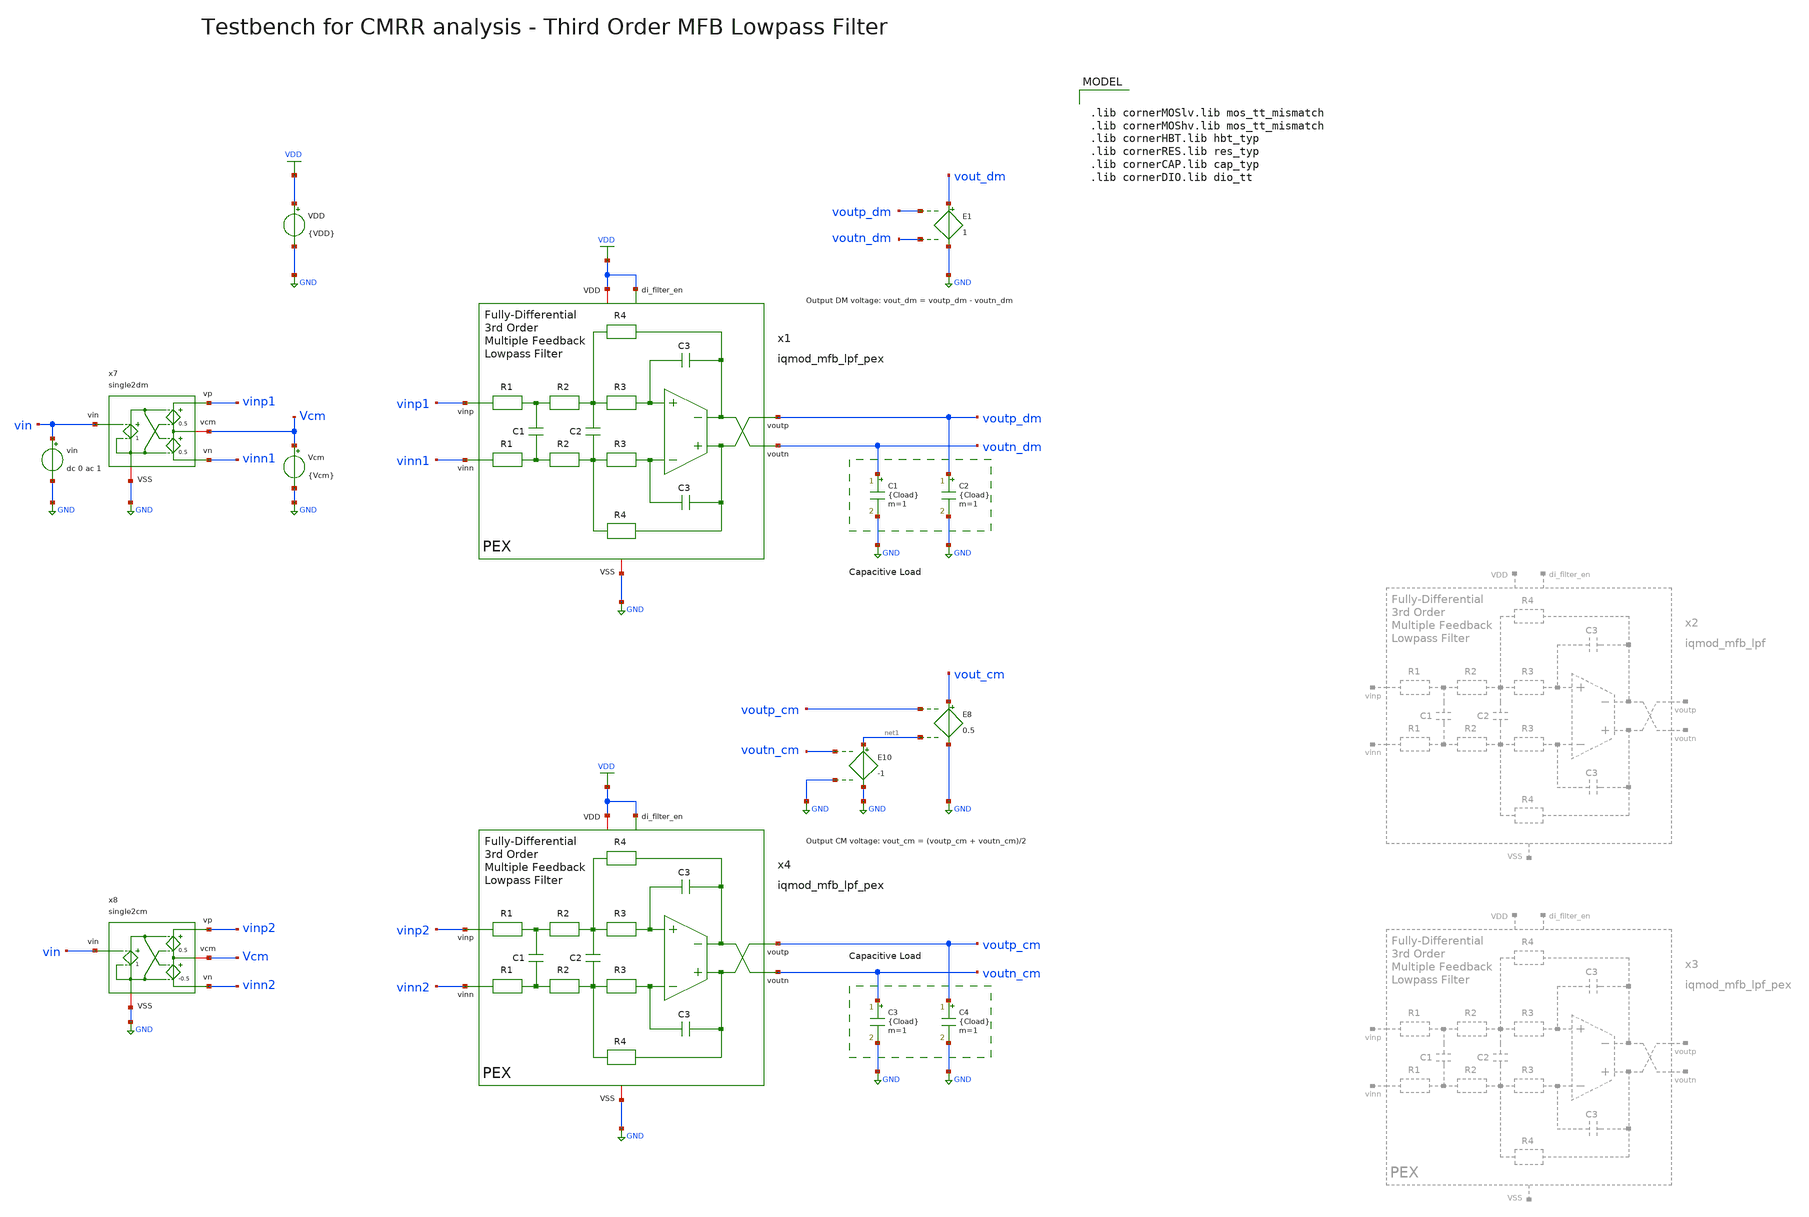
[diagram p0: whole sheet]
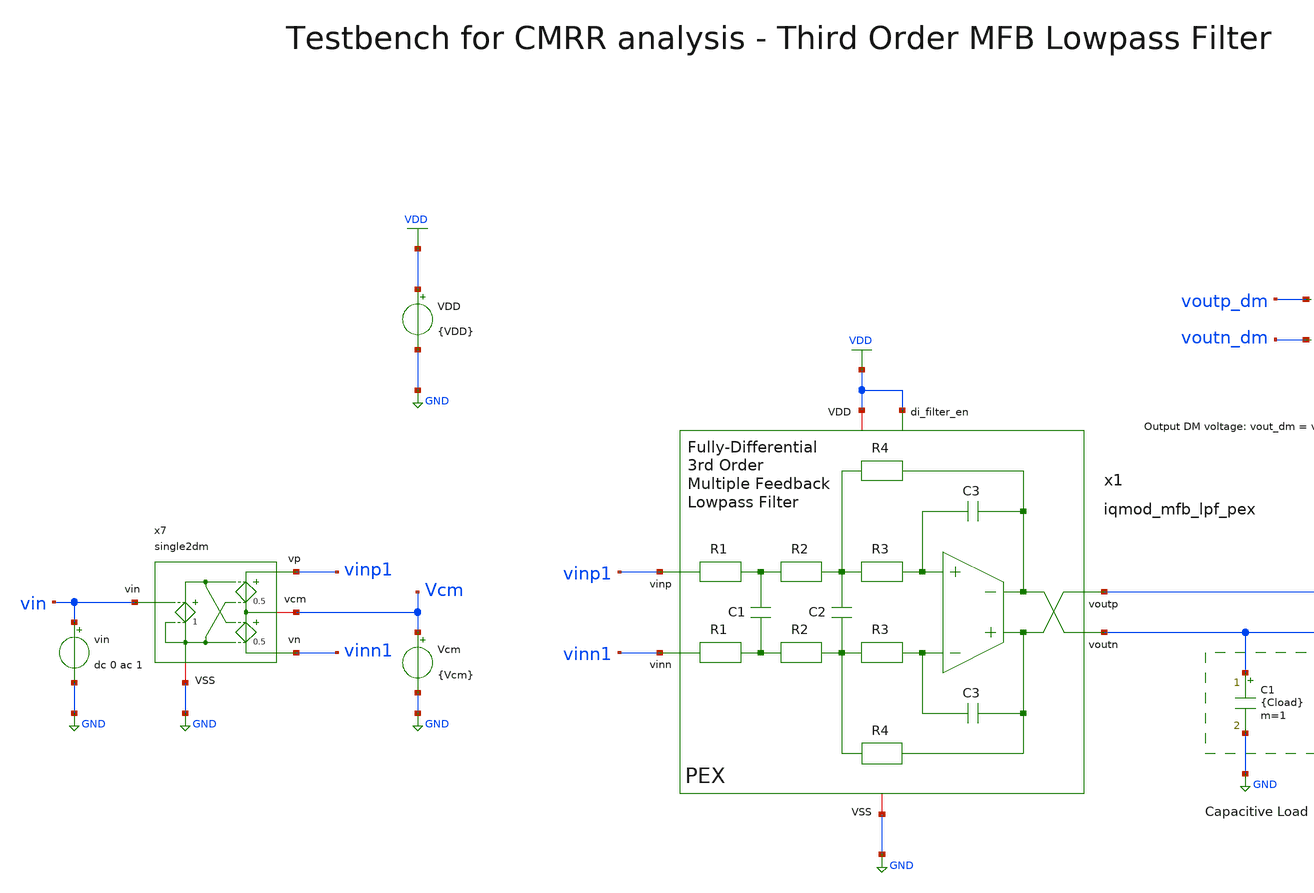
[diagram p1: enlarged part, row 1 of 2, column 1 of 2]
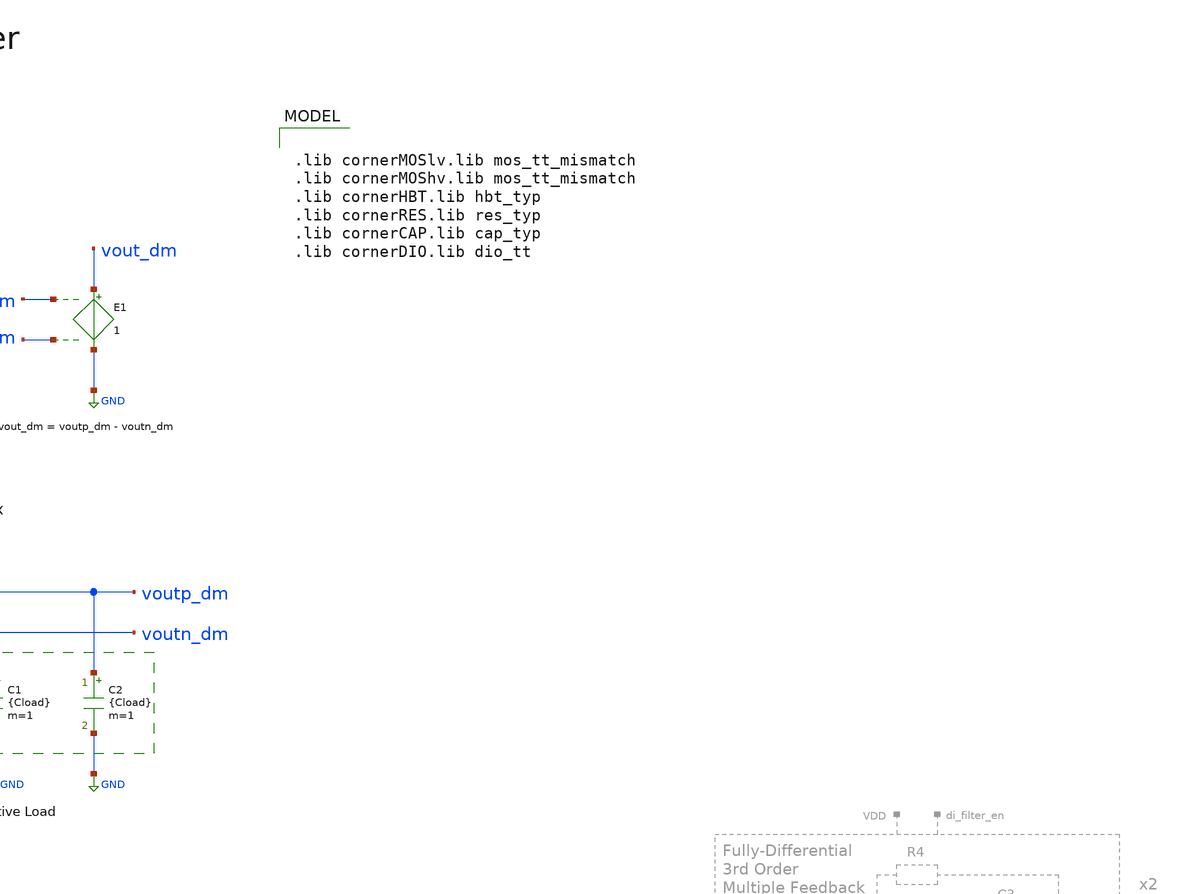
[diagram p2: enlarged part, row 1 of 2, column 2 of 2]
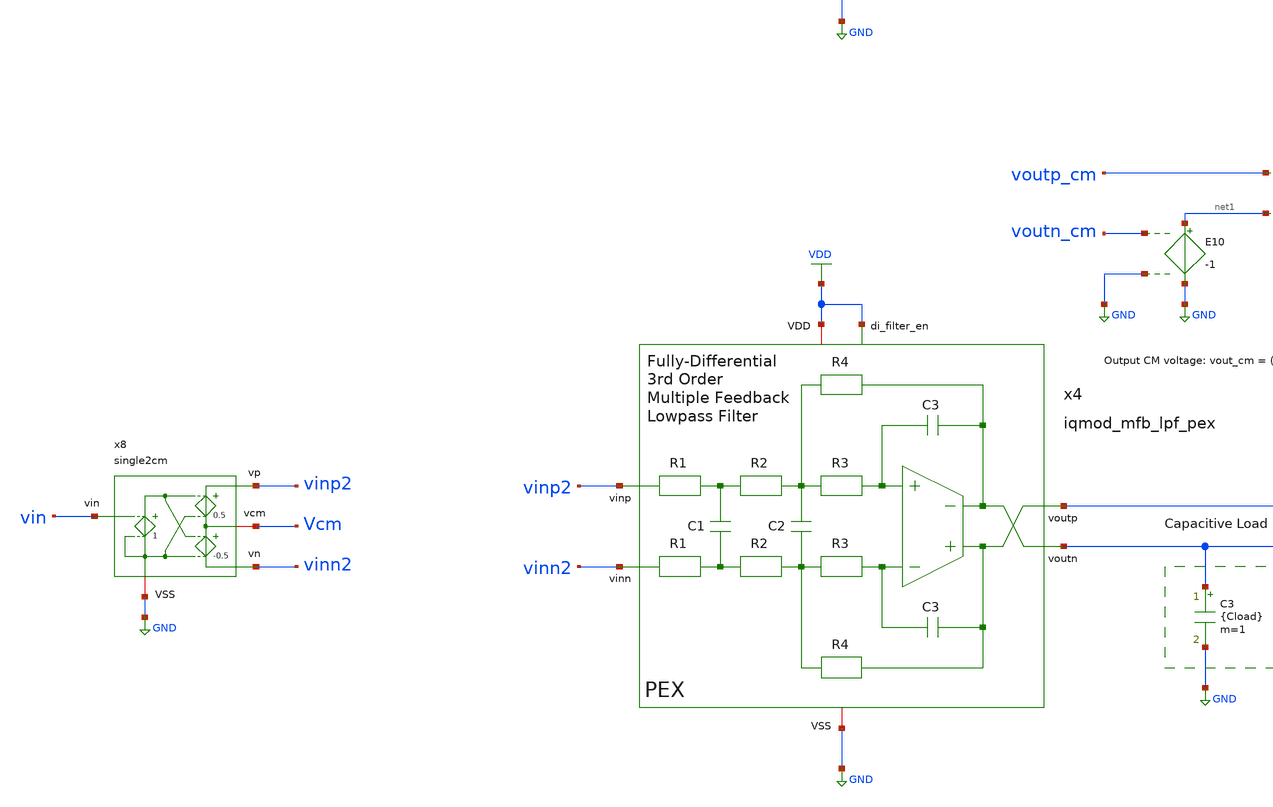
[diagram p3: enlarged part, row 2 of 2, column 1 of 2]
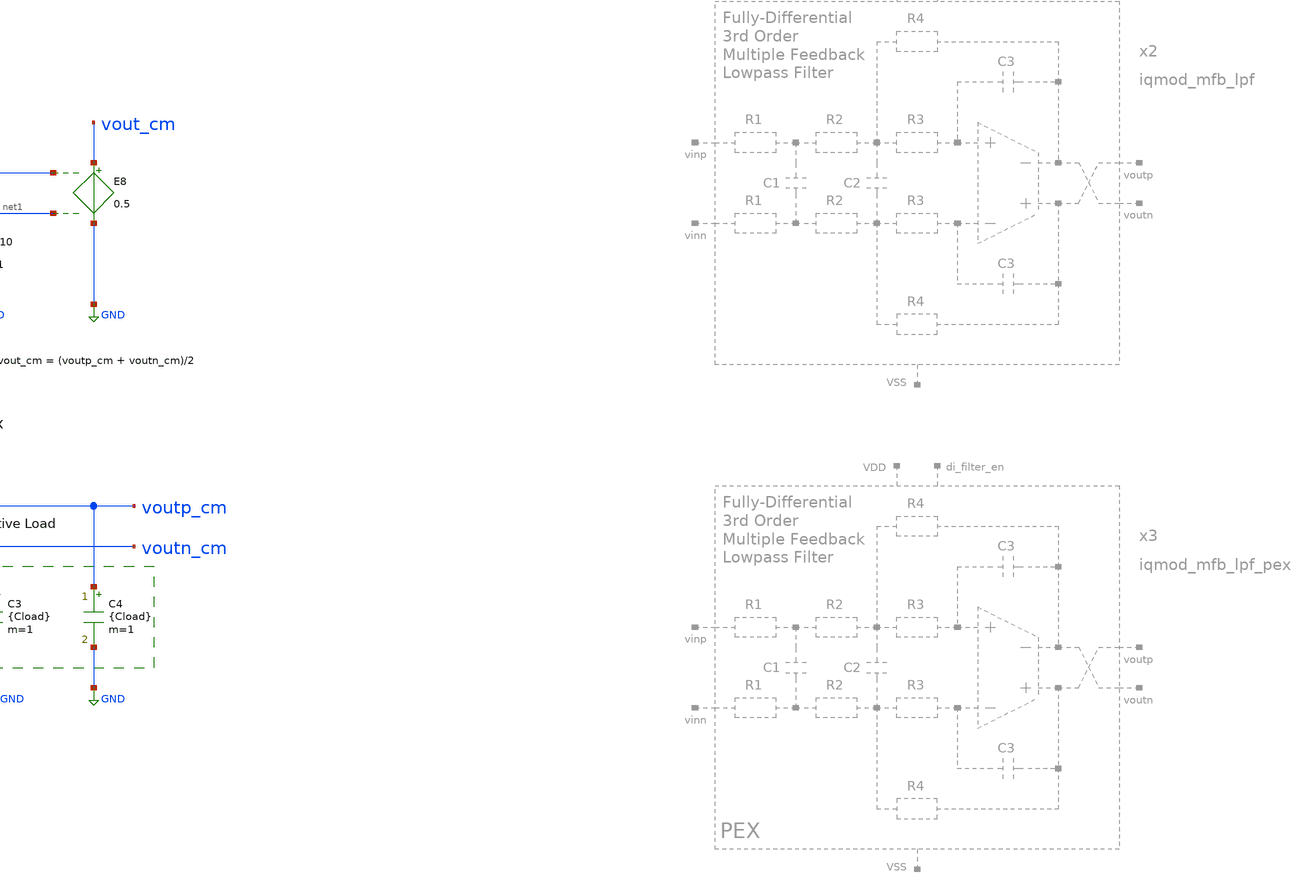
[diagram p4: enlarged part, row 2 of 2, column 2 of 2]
** sch_path: ihp130/macros/iqmod/xschem/testbenches/iqmod_mfb_lpf_tb_CMRR.sch
**.subckt iqmod_mfb_lpf_tb_CMRR
C1 voutn_dm GND {Cload} m=1
C2 voutp_dm GND {Cload} m=1
Vcm Vcm GND {Vcm}
E1 vout_dm GND voutp_dm voutn_dm 1
vin vin GND dc 0 ac 1
C3 voutn_cm GND {Cload} m=1
C4 voutp_cm GND {Cload} m=1
E8 vout_cm GND voutp_cm net1 0.5
E10 net1 GND voutn_cm GND -1
x7 vinp1 vin Vcm GND vinn1 single2dm
x8 vinp2 vin Vcm GND vinn2 single2cm
VDD VDD GND {VDD}
x1 voutp_dm vinp1 voutn_dm vinn1 VDD GND VDD iqmod_mfb_lpf_pex
x4 voutp_cm vinp2 voutn_cm vinn2 VDD GND VDD iqmod_mfb_lpf_pex
**** begin user architecture code


.include ../../verification/pex/iqmod_mfb_lpf_pex.spice
.param VDD=1.5
.param Vcm=VDD/2
.param temp=27
.param Cload=10p
.param vphi=0.5
.param f_min = 10m
.csparam f_min = f_min
.param f_max = 1G
.csparam f_max = f_max
.param fdc = 10
.csparam fdc = fdc
.options savecurrents klu method=gear reltol=1e-3 abstol=1e-12 gmin=1e-12 rshunt=1e12
.control

* save v(vout_dm) v(vout_cm) v(vin)
save all

set wr_vecnames
set wr_singlescale

* User Constants
let f_min = 0.1
let f_max = 1G
let fdc = 1

* Operating Point Analysis
op
remzerovec
write iqmod_mfb_lpf_tb_CMRR.raw
set appendwrite

* AC Analysis
ac dec 101 $&const.f_min $&const.f_max
remzerovec
write iqmod_mfb_lpf_tb_CMRR.raw

* Plotting Differential Mode Gain
let Adm = v(vout_dm)/v(vin)
let Adm_dB = vdb(Adm)
let Adm_arg = 180/PI*cphase(Adm)
plot Adm_dB Adm_arg ylabel 'Magnitude, Phase'

* Plotting Common Mode Gain
let Acm = v(vout_cm)/v(vin)
let Acm_dB = vdb(Acm)
let Acm_arg = 180/PI*cphase(Acm)
plot Acm_dB Acm_arg ylabel 'Magnitude, Phase'

* Plotting Common Mode Rejection Ratio
* let CMRR = v(vout_dm)/v(vout_cm)
let CMRR = v(Adm)/v(Acm)
let CMRR_dB = vdb(CMRR)
* let CMRR_dB = Adm_dB - Acm_dB
let CMRR_arg = 180/PI*cphase(CMRR)
plot CMRR_dB CMRR_arg ylabel 'Magnitude, Phase'

* Measurements
meas ac CMRRdc_dB find CMRR_dB when frequency = fdc
print CMRRdc_dB

* Write Data
unset appendwrite
set wr_vecnames
set wr_singlescale
wrdata $PROJECT_PATH/python/plot_simulations/data/iqmod_mfb_lpf_tb_CMRR.txt v(Adm_dB) v(Adm_arg)
+ v(Acm_dB) v(Acm_arg) v(CMRR_dB) v(CMRR_arg)

*quit
.endc



.lib cornerMOSlv.lib mos_tt_mismatch
.lib cornerMOShv.lib mos_tt_mismatch
.lib cornerHBT.lib hbt_typ
.lib cornerRES.lib res_typ
.lib cornerCAP.lib cap_typ
.lib cornerDIO.lib dio_tt

**** end user architecture code
**.ends
.GLOBAL GND
.GLOBAL VDD
.end
